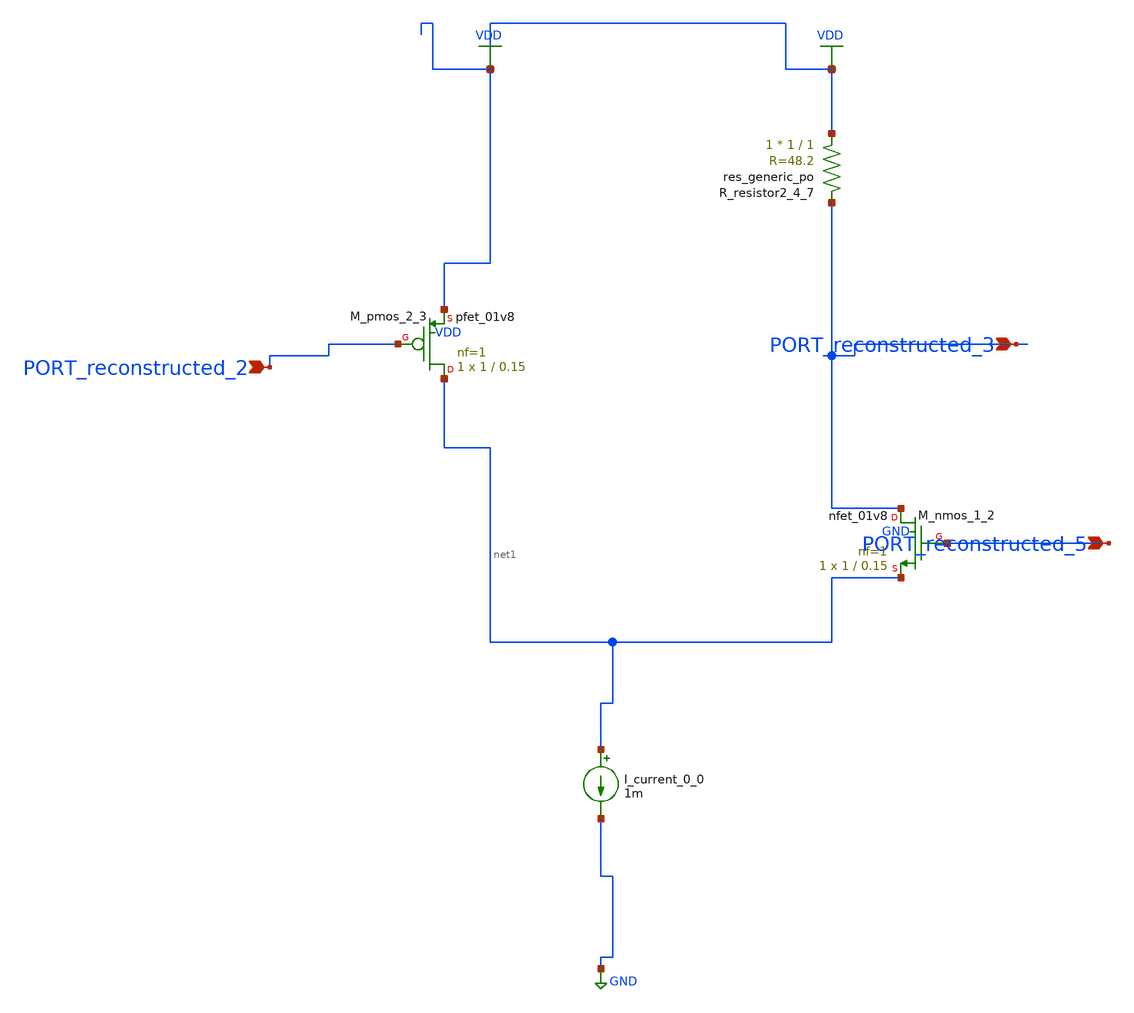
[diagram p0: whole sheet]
** sch_path: schematics/AMSNet/141.sch
**.subckt 141 PORT_reconstructed_5 PORT_reconstructed_2 PORT_reconstructed_3
*.ipin PORT_reconstructed_5
*.ipin PORT_reconstructed_2
*.ipin PORT_reconstructed_3
I_current_0_0 net1 GND 1m
XM_nmos_1_2 PORT_reconstructed_3 PORT_reconstructed_5 net1 GND sky130_fd_pr__nfet_01v8 L=0.15 W=1 nf=1
+ ad='int((1 + 1)/2) * 1 / 1 * 0.29' as='int((1 + 2)/2) * 1 / 1 * 0.29' pd='2*int((1 + 1)/2) * (1 / 1 + 0.29)'
+ ps='2*int((1 + 2)/2) * (1 / 1 + 0.29)' nrd='0.29 / 1 ' nrs='0.29 / 1 ' sa=0 sb=0 sd=0 mult=1 m=1
XM_pmos_2_3 net1 PORT_reconstructed_2 VDD VDD sky130_fd_pr__pfet_01v8 L=0.15 W=1 nf=1 ad='int((1 + 1)/2) * 1 / 1 * 0.29'
+ as='int((1 + 2)/2) * 1 / 1 * 0.29' pd='2*int((1 + 1)/2) * (1 / 1 + 0.29)' ps='2*int((1 + 2)/2) * (1 / 1 + 0.29)'
+ nrd='0.29 / 1 ' nrs='0.29 / 1 ' sa=0 sb=0 sd=0 mult=1 m=1
XR_resistor2_4_7 VDD PORT_reconstructed_3 sky130_fd_pr__res_generic_po W=1 L=1 m=1
**.ends
.GLOBAL GND
.GLOBAL VDD
.end
